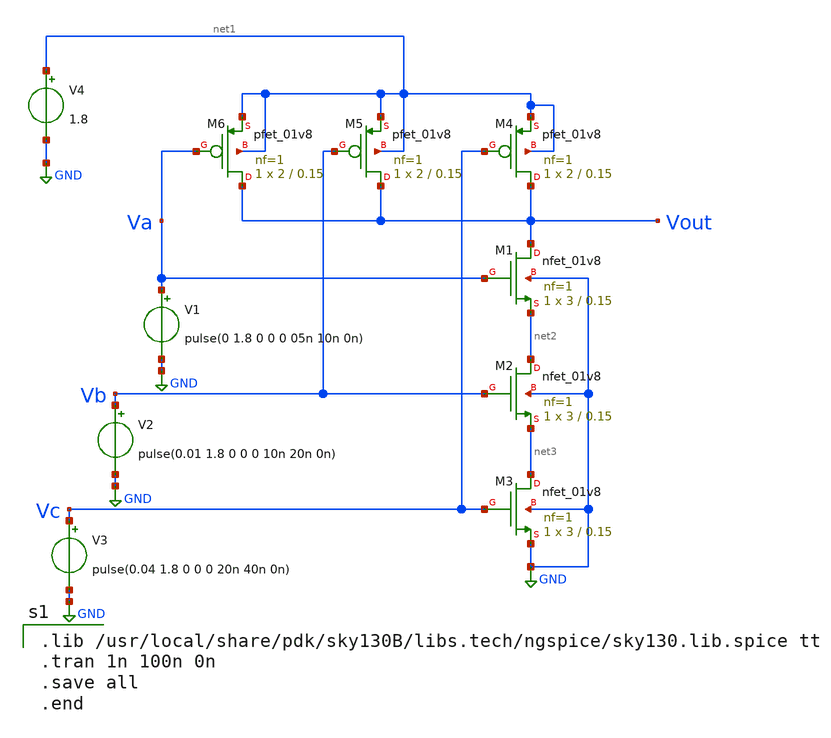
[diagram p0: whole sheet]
** sch_path: 3_input_nand_gate/nand3_gate.sch
**.subckt nand3_gate
XM1 Vout Va net2 GND sky130_fd_pr__nfet_01v8 L=0.15 W=3 nf=1 ad='int((nf+1)/2) * W/nf * 0.29' as='int((nf+2)/2) * W/nf * 0.29'
+ pd='2*int((nf+1)/2) * (W/nf + 0.29)' ps='2*int((nf+2)/2) * (W/nf + 0.29)' nrd='0.29 / W' nrs='0.29 / W'
+ sa=0 sb=0 sd=0 mult=1 m=1
XM2 net2 Vb net3 GND sky130_fd_pr__nfet_01v8 L=0.15 W=3 nf=1 ad='int((nf+1)/2) * W/nf * 0.29' as='int((nf+2)/2) * W/nf * 0.29'
+ pd='2*int((nf+1)/2) * (W/nf + 0.29)' ps='2*int((nf+2)/2) * (W/nf + 0.29)' nrd='0.29 / W' nrs='0.29 / W'
+ sa=0 sb=0 sd=0 mult=1 m=1
XM3 net3 Vc GND GND sky130_fd_pr__nfet_01v8 L=0.15 W=3 nf=1 ad='int((nf+1)/2) * W/nf * 0.29' as='int((nf+2)/2) * W/nf * 0.29'
+ pd='2*int((nf+1)/2) * (W/nf + 0.29)' ps='2*int((nf+2)/2) * (W/nf + 0.29)' nrd='0.29 / W' nrs='0.29 / W'
+ sa=0 sb=0 sd=0 mult=1 m=1
XM4 Vout Vc net1 net1 sky130_fd_pr__pfet_01v8 L=0.15 W=2 nf=1 ad='int((nf+1)/2) * W/nf * 0.29' as='int((nf+2)/2) * W/nf * 0.29'
+ pd='2*int((nf+1)/2) * (W/nf + 0.29)' ps='2*int((nf+2)/2) * (W/nf + 0.29)' nrd='0.29 / W' nrs='0.29 / W'
+ sa=0 sb=0 sd=0 mult=1 m=1
XM5 Vout Vb net1 net1 sky130_fd_pr__pfet_01v8 L=0.15 W=2 nf=1 ad='int((nf+1)/2) * W/nf * 0.29' as='int((nf+2)/2) * W/nf * 0.29'
+ pd='2*int((nf+1)/2) * (W/nf + 0.29)' ps='2*int((nf+2)/2) * (W/nf + 0.29)' nrd='0.29 / W' nrs='0.29 / W'
+ sa=0 sb=0 sd=0 mult=1 m=1
XM6 Vout Va net1 net1 sky130_fd_pr__pfet_01v8 L=0.15 W=2 nf=1 ad='int((nf+1)/2) * W/nf * 0.29' as='int((nf+2)/2) * W/nf * 0.29'
+ pd='2*int((nf+1)/2) * (W/nf + 0.29)' ps='2*int((nf+2)/2) * (W/nf + 0.29)' nrd='0.29 / W' nrs='0.29 / W'
+ sa=0 sb=0 sd=0 mult=1 m=1
V1 Va GND pulse(0 1.8 0 0 0 05n 10n 0n)
V2 Vb GND pulse(0.01 1.8 0 0 0 10n 20n 0n)
V3 Vc GND pulse(0.04 1.8 0 0 0 20n 40n 0n)
V4 net1 GND 1.8
**** begin user architecture code

.lib /usr/local/share/pdk/sky130B/libs.tech/ngspice/sky130.lib.spice tt
.tran 1n 100n 0n
.save all
.end

**** end user architecture code
**.ends
.GLOBAL GND
.end
